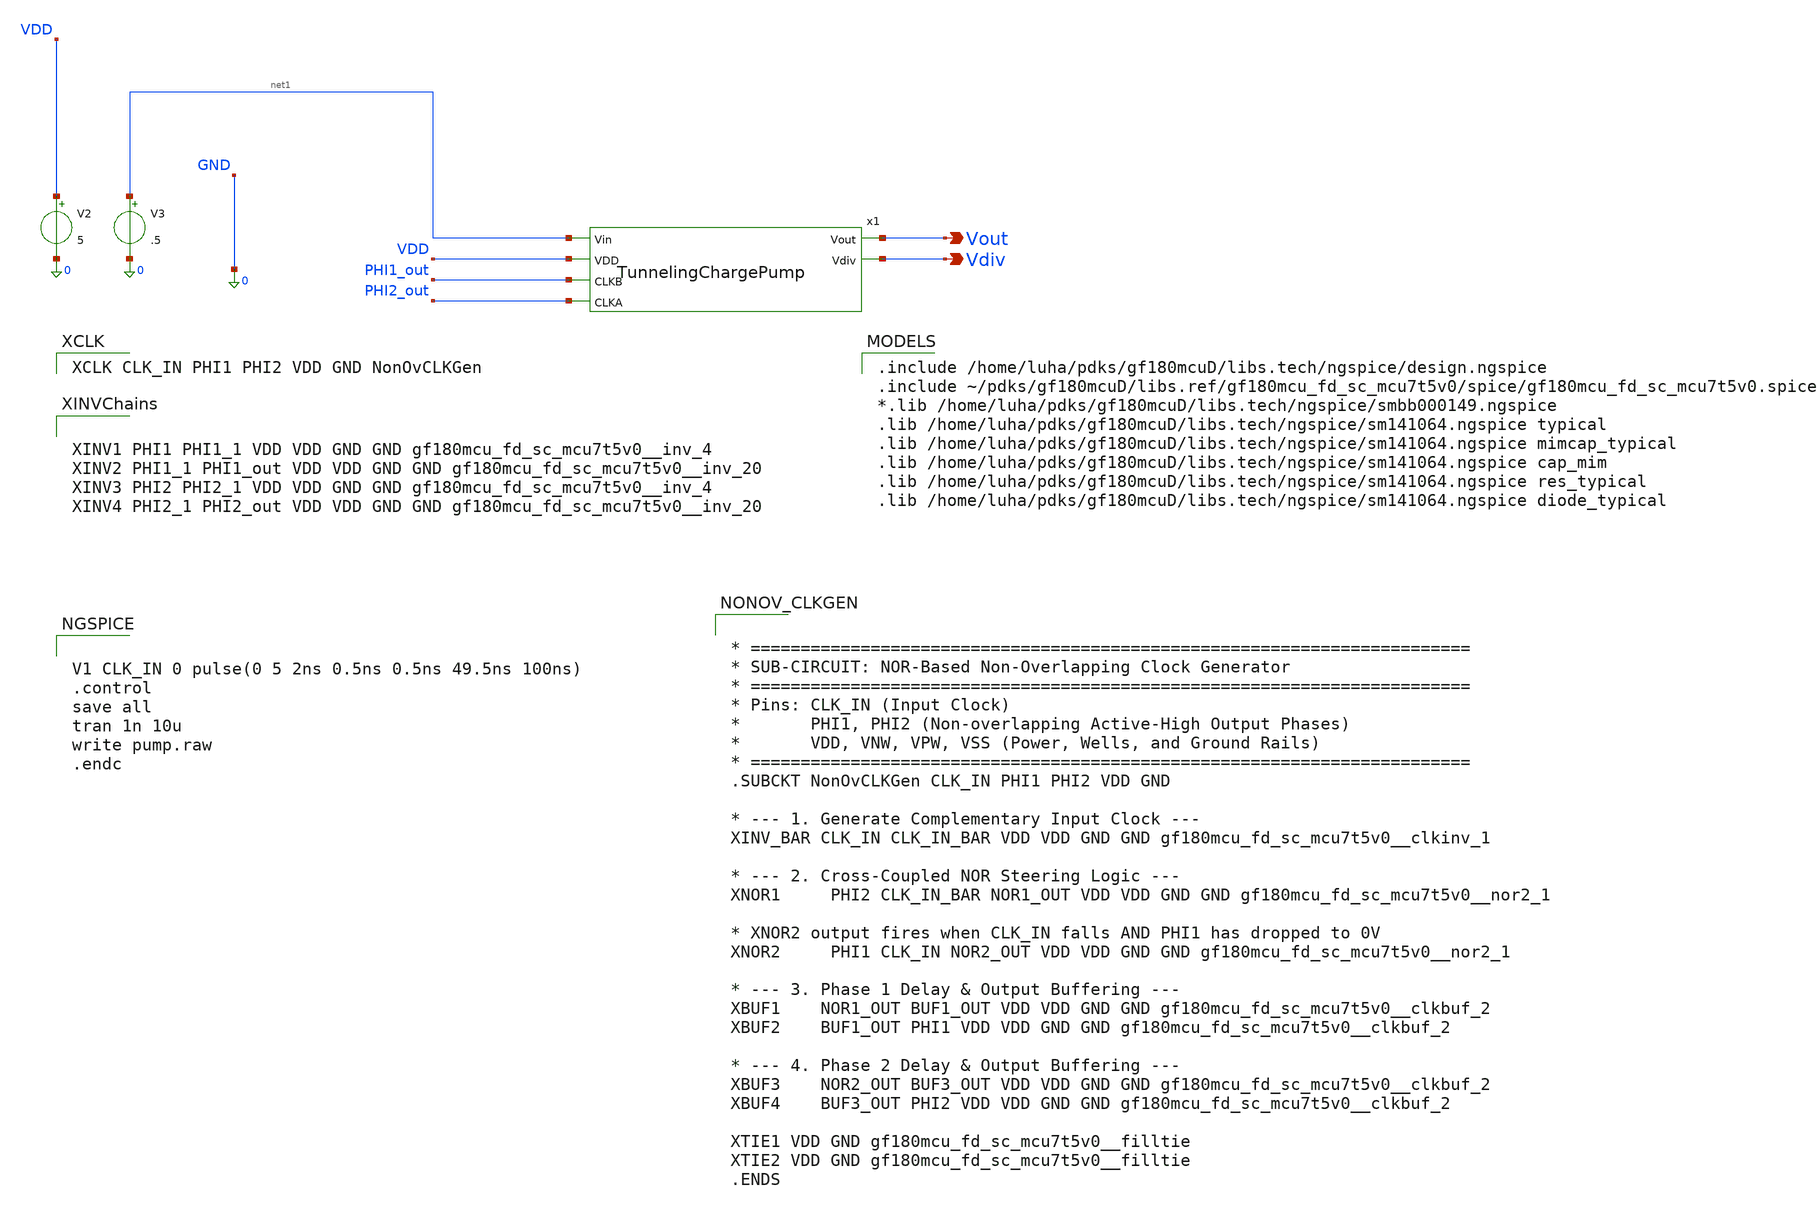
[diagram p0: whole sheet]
** sch_path: 1_Design/GF180_cells/TunnelingChargePump/TunnelingChargePump_TB.sch
**.subckt TunnelingChargePump_TB Vout Vdiv
*.opin Vout
*.opin Vdiv
V2 VDD 0 5
V3 net1 0 .5
x1 net1 Vout Vdiv VDD PHI1_out PHI2_out TunnelingChargePump
**** begin user architecture code
 .include /home/luha/pdks/gf180mcuD/libs.tech/ngspice/design.ngspice
.include ~/pdks/gf180mcuD/libs.ref/gf180mcu_fd_sc_mcu7t5v0/spice/gf180mcu_fd_sc_mcu7t5v0.spice
*.lib /home/luha/pdks/gf180mcuD/libs.tech/ngspice/smbb000149.ngspice
.lib /home/luha/pdks/gf180mcuD/libs.tech/ngspice/sm141064.ngspice typical
.lib /home/luha/pdks/gf180mcuD/libs.tech/ngspice/sm141064.ngspice mimcap_typical
.lib /home/luha/pdks/gf180mcuD/libs.tech/ngspice/sm141064.ngspice cap_mim
.lib /home/luha/pdks/gf180mcuD/libs.tech/ngspice/sm141064.ngspice res_typical
.lib /home/luha/pdks/gf180mcuD/libs.tech/ngspice/sm141064.ngspice diode_typical



V1 CLK_IN 0 pulse(0 5 2ns 0.5ns 0.5ns 49.5ns 100ns)
.control
save all
tran 1n 10u
write pump.raw
.endc




* ========================================================================
* SUB-CIRCUIT: NOR-Based Non-Overlapping Clock Generator
* ========================================================================
* Pins: CLK_IN (Input Clock)
*       PHI1, PHI2 (Non-overlapping Active-High Output Phases)
*       VDD, VNW, VPW, VSS (Power, Wells, and Ground Rails)
* ========================================================================
.SUBCKT NonOvCLKGen CLK_IN PHI1 PHI2 VDD GND

* --- 1. Generate Complementary Input Clock ---
XINV_BAR CLK_IN CLK_IN_BAR VDD VDD GND GND gf180mcu_fd_sc_mcu7t5v0__clkinv_1

* --- 2. Cross-Coupled NOR Steering Logic ---
XNOR1	 PHI2 CLK_IN_BAR NOR1_OUT VDD VDD GND GND gf180mcu_fd_sc_mcu7t5v0__nor2_1

* XNOR2 output fires when CLK_IN falls AND PHI1 has dropped to 0V
XNOR2	 PHI1 CLK_IN NOR2_OUT VDD VDD GND GND gf180mcu_fd_sc_mcu7t5v0__nor2_1

* --- 3. Phase 1 Delay & Output Buffering ---
XBUF1    NOR1_OUT BUF1_OUT VDD VDD GND GND gf180mcu_fd_sc_mcu7t5v0__clkbuf_2
XBUF2    BUF1_OUT PHI1 VDD VDD GND GND gf180mcu_fd_sc_mcu7t5v0__clkbuf_2

* --- 4. Phase 2 Delay & Output Buffering ---
XBUF3    NOR2_OUT BUF3_OUT VDD VDD GND GND gf180mcu_fd_sc_mcu7t5v0__clkbuf_2
XBUF4    BUF3_OUT PHI2 VDD VDD GND GND gf180mcu_fd_sc_mcu7t5v0__clkbuf_2

XTIE1 VDD GND gf180mcu_fd_sc_mcu7t5v0__filltie
XTIE2 VDD GND gf180mcu_fd_sc_mcu7t5v0__filltie
.ENDS



XCLK CLK_IN PHI1 PHI2 VDD GND NonOvCLKGen



XINV1 PHI1 PHI1_1 VDD VDD GND GND gf180mcu_fd_sc_mcu7t5v0__inv_4
XINV2 PHI1_1 PHI1_out VDD VDD GND GND gf180mcu_fd_sc_mcu7t5v0__inv_20
XINV3 PHI2 PHI2_1 VDD VDD GND GND gf180mcu_fd_sc_mcu7t5v0__inv_4
XINV4 PHI2_1 PHI2_out VDD VDD GND GND gf180mcu_fd_sc_mcu7t5v0__inv_20



**** end user architecture code
**.ends
.end
